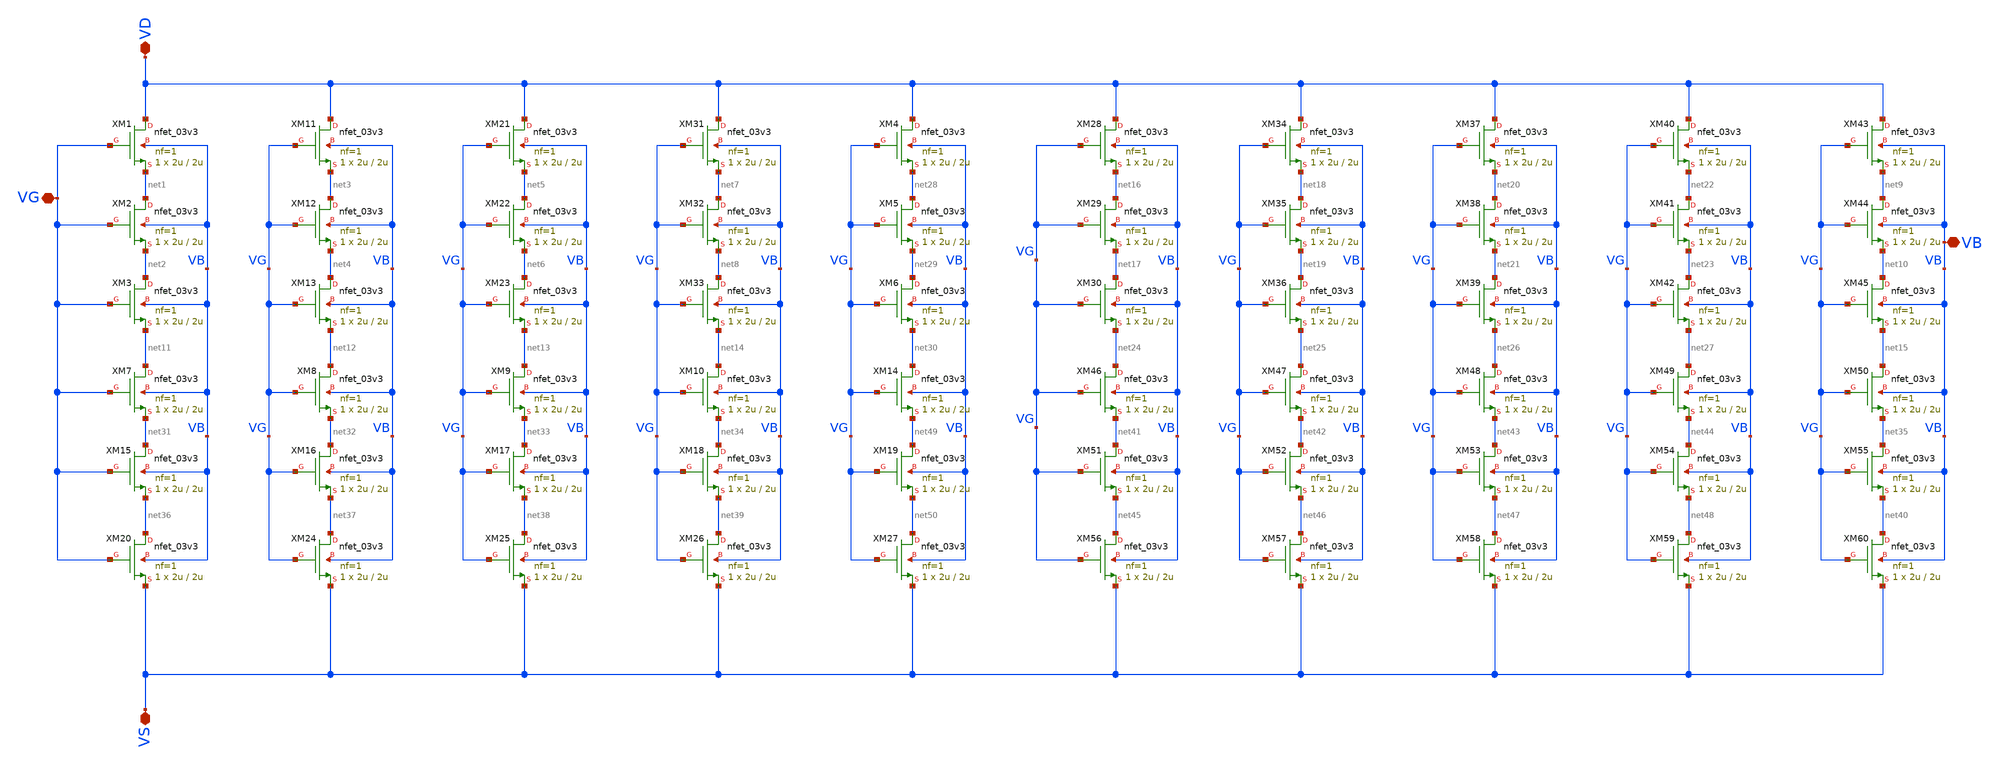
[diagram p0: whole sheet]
** sch_path: Voltage_Reference/symbols/NMOS_association_10u_6u_V2.sch
**.subckt NMOS_association_10u_6u_V2 VD VB VG VS
*.iopin VD
*.iopin VB
*.iopin VG
*.iopin VS
XM1 VD VG net1 VB nfet_03v3 L=2u W=2u nf=1 ad='int((nf+1)/2) * W/nf * 0.18u' as='int((nf+2)/2) * W/nf * 0.18u'
+ pd='2*int((nf+1)/2) * (W/nf + 0.18u)' ps='2*int((nf+2)/2) * (W/nf + 0.18u)' nrd='0.18u / W' nrs='0.18u / W'
+ sa=0 sb=0 sd=0 m=1
XM2 net1 VG net2 VB nfet_03v3 L=2u W=2u nf=1 ad='int((nf+1)/2) * W/nf * 0.18u' as='int((nf+2)/2) * W/nf * 0.18u'
+ pd='2*int((nf+1)/2) * (W/nf + 0.18u)' ps='2*int((nf+2)/2) * (W/nf + 0.18u)' nrd='0.18u / W' nrs='0.18u / W'
+ sa=0 sb=0 sd=0 m=1
XM3 net2 VG net11 VB nfet_03v3 L=2u W=2u nf=1 ad='int((nf+1)/2) * W/nf * 0.18u' as='int((nf+2)/2) * W/nf * 0.18u'
+ pd='2*int((nf+1)/2) * (W/nf + 0.18u)' ps='2*int((nf+2)/2) * (W/nf + 0.18u)' nrd='0.18u / W' nrs='0.18u / W'
+ sa=0 sb=0 sd=0 m=1
XM11 VD VG net3 VB nfet_03v3 L=2u W=2u nf=1 ad='int((nf+1)/2) * W/nf * 0.18u' as='int((nf+2)/2) * W/nf * 0.18u'
+ pd='2*int((nf+1)/2) * (W/nf + 0.18u)' ps='2*int((nf+2)/2) * (W/nf + 0.18u)' nrd='0.18u / W' nrs='0.18u / W'
+ sa=0 sb=0 sd=0 m=1
XM12 net3 VG net4 VB nfet_03v3 L=2u W=2u nf=1 ad='int((nf+1)/2) * W/nf * 0.18u' as='int((nf+2)/2) * W/nf * 0.18u'
+ pd='2*int((nf+1)/2) * (W/nf + 0.18u)' ps='2*int((nf+2)/2) * (W/nf + 0.18u)' nrd='0.18u / W' nrs='0.18u / W'
+ sa=0 sb=0 sd=0 m=1
XM13 net4 VG net12 VB nfet_03v3 L=2u W=2u nf=1 ad='int((nf+1)/2) * W/nf * 0.18u' as='int((nf+2)/2) * W/nf * 0.18u'
+ pd='2*int((nf+1)/2) * (W/nf + 0.18u)' ps='2*int((nf+2)/2) * (W/nf + 0.18u)' nrd='0.18u / W' nrs='0.18u / W'
+ sa=0 sb=0 sd=0 m=1
XM21 VD VG net5 VB nfet_03v3 L=2u W=2u nf=1 ad='int((nf+1)/2) * W/nf * 0.18u' as='int((nf+2)/2) * W/nf * 0.18u'
+ pd='2*int((nf+1)/2) * (W/nf + 0.18u)' ps='2*int((nf+2)/2) * (W/nf + 0.18u)' nrd='0.18u / W' nrs='0.18u / W'
+ sa=0 sb=0 sd=0 m=1
XM22 net5 VG net6 VB nfet_03v3 L=2u W=2u nf=1 ad='int((nf+1)/2) * W/nf * 0.18u' as='int((nf+2)/2) * W/nf * 0.18u'
+ pd='2*int((nf+1)/2) * (W/nf + 0.18u)' ps='2*int((nf+2)/2) * (W/nf + 0.18u)' nrd='0.18u / W' nrs='0.18u / W'
+ sa=0 sb=0 sd=0 m=1
XM23 net6 VG net13 VB nfet_03v3 L=2u W=2u nf=1 ad='int((nf+1)/2) * W/nf * 0.18u' as='int((nf+2)/2) * W/nf * 0.18u'
+ pd='2*int((nf+1)/2) * (W/nf + 0.18u)' ps='2*int((nf+2)/2) * (W/nf + 0.18u)' nrd='0.18u / W' nrs='0.18u / W'
+ sa=0 sb=0 sd=0 m=1
XM31 VD VG net7 VB nfet_03v3 L=2u W=2u nf=1 ad='int((nf+1)/2) * W/nf * 0.18u' as='int((nf+2)/2) * W/nf * 0.18u'
+ pd='2*int((nf+1)/2) * (W/nf + 0.18u)' ps='2*int((nf+2)/2) * (W/nf + 0.18u)' nrd='0.18u / W' nrs='0.18u / W'
+ sa=0 sb=0 sd=0 m=1
XM32 net7 VG net8 VB nfet_03v3 L=2u W=2u nf=1 ad='int((nf+1)/2) * W/nf * 0.18u' as='int((nf+2)/2) * W/nf * 0.18u'
+ pd='2*int((nf+1)/2) * (W/nf + 0.18u)' ps='2*int((nf+2)/2) * (W/nf + 0.18u)' nrd='0.18u / W' nrs='0.18u / W'
+ sa=0 sb=0 sd=0 m=1
XM33 net8 VG net14 VB nfet_03v3 L=2u W=2u nf=1 ad='int((nf+1)/2) * W/nf * 0.18u' as='int((nf+2)/2) * W/nf * 0.18u'
+ pd='2*int((nf+1)/2) * (W/nf + 0.18u)' ps='2*int((nf+2)/2) * (W/nf + 0.18u)' nrd='0.18u / W' nrs='0.18u / W'
+ sa=0 sb=0 sd=0 m=1
XM4 VD VG net28 VB nfet_03v3 L=2u W=2u nf=1 ad='int((nf+1)/2) * W/nf * 0.18u' as='int((nf+2)/2) * W/nf * 0.18u'
+ pd='2*int((nf+1)/2) * (W/nf + 0.18u)' ps='2*int((nf+2)/2) * (W/nf + 0.18u)' nrd='0.18u / W' nrs='0.18u / W'
+ sa=0 sb=0 sd=0 m=1
XM5 net28 VG net29 VB nfet_03v3 L=2u W=2u nf=1 ad='int((nf+1)/2) * W/nf * 0.18u' as='int((nf+2)/2) * W/nf * 0.18u'
+ pd='2*int((nf+1)/2) * (W/nf + 0.18u)' ps='2*int((nf+2)/2) * (W/nf + 0.18u)' nrd='0.18u / W' nrs='0.18u / W'
+ sa=0 sb=0 sd=0 m=1
XM6 net29 VG net30 VB nfet_03v3 L=2u W=2u nf=1 ad='int((nf+1)/2) * W/nf * 0.18u' as='int((nf+2)/2) * W/nf * 0.18u'
+ pd='2*int((nf+1)/2) * (W/nf + 0.18u)' ps='2*int((nf+2)/2) * (W/nf + 0.18u)' nrd='0.18u / W' nrs='0.18u / W'
+ sa=0 sb=0 sd=0 m=1
XM7 net11 VG net31 VB nfet_03v3 L=2u W=2u nf=1 ad='int((nf+1)/2) * W/nf * 0.18u' as='int((nf+2)/2) * W/nf * 0.18u'
+ pd='2*int((nf+1)/2) * (W/nf + 0.18u)' ps='2*int((nf+2)/2) * (W/nf + 0.18u)' nrd='0.18u / W' nrs='0.18u / W'
+ sa=0 sb=0 sd=0 m=1
XM8 net12 VG net32 VB nfet_03v3 L=2u W=2u nf=1 ad='int((nf+1)/2) * W/nf * 0.18u' as='int((nf+2)/2) * W/nf * 0.18u'
+ pd='2*int((nf+1)/2) * (W/nf + 0.18u)' ps='2*int((nf+2)/2) * (W/nf + 0.18u)' nrd='0.18u / W' nrs='0.18u / W'
+ sa=0 sb=0 sd=0 m=1
XM9 net13 VG net33 VB nfet_03v3 L=2u W=2u nf=1 ad='int((nf+1)/2) * W/nf * 0.18u' as='int((nf+2)/2) * W/nf * 0.18u'
+ pd='2*int((nf+1)/2) * (W/nf + 0.18u)' ps='2*int((nf+2)/2) * (W/nf + 0.18u)' nrd='0.18u / W' nrs='0.18u / W'
+ sa=0 sb=0 sd=0 m=1
XM10 net14 VG net34 VB nfet_03v3 L=2u W=2u nf=1 ad='int((nf+1)/2) * W/nf * 0.18u' as='int((nf+2)/2) * W/nf * 0.18u'
+ pd='2*int((nf+1)/2) * (W/nf + 0.18u)' ps='2*int((nf+2)/2) * (W/nf + 0.18u)' nrd='0.18u / W' nrs='0.18u / W'
+ sa=0 sb=0 sd=0 m=1
XM14 net30 VG net49 VB nfet_03v3 L=2u W=2u nf=1 ad='int((nf+1)/2) * W/nf * 0.18u' as='int((nf+2)/2) * W/nf * 0.18u'
+ pd='2*int((nf+1)/2) * (W/nf + 0.18u)' ps='2*int((nf+2)/2) * (W/nf + 0.18u)' nrd='0.18u / W' nrs='0.18u / W'
+ sa=0 sb=0 sd=0 m=1
XM28 VD VG net16 VB nfet_03v3 L=2u W=2u nf=1 ad='int((nf+1)/2) * W/nf * 0.18u' as='int((nf+2)/2) * W/nf * 0.18u'
+ pd='2*int((nf+1)/2) * (W/nf + 0.18u)' ps='2*int((nf+2)/2) * (W/nf + 0.18u)' nrd='0.18u / W' nrs='0.18u / W'
+ sa=0 sb=0 sd=0 m=1
XM29 net16 VG net17 VB nfet_03v3 L=2u W=2u nf=1 ad='int((nf+1)/2) * W/nf * 0.18u' as='int((nf+2)/2) * W/nf * 0.18u'
+ pd='2*int((nf+1)/2) * (W/nf + 0.18u)' ps='2*int((nf+2)/2) * (W/nf + 0.18u)' nrd='0.18u / W' nrs='0.18u / W'
+ sa=0 sb=0 sd=0 m=1
XM30 net17 VG net24 VB nfet_03v3 L=2u W=2u nf=1 ad='int((nf+1)/2) * W/nf * 0.18u' as='int((nf+2)/2) * W/nf * 0.18u'
+ pd='2*int((nf+1)/2) * (W/nf + 0.18u)' ps='2*int((nf+2)/2) * (W/nf + 0.18u)' nrd='0.18u / W' nrs='0.18u / W'
+ sa=0 sb=0 sd=0 m=1
XM34 VD VG net18 VB nfet_03v3 L=2u W=2u nf=1 ad='int((nf+1)/2) * W/nf * 0.18u' as='int((nf+2)/2) * W/nf * 0.18u'
+ pd='2*int((nf+1)/2) * (W/nf + 0.18u)' ps='2*int((nf+2)/2) * (W/nf + 0.18u)' nrd='0.18u / W' nrs='0.18u / W'
+ sa=0 sb=0 sd=0 m=1
XM35 net18 VG net19 VB nfet_03v3 L=2u W=2u nf=1 ad='int((nf+1)/2) * W/nf * 0.18u' as='int((nf+2)/2) * W/nf * 0.18u'
+ pd='2*int((nf+1)/2) * (W/nf + 0.18u)' ps='2*int((nf+2)/2) * (W/nf + 0.18u)' nrd='0.18u / W' nrs='0.18u / W'
+ sa=0 sb=0 sd=0 m=1
XM36 net19 VG net25 VB nfet_03v3 L=2u W=2u nf=1 ad='int((nf+1)/2) * W/nf * 0.18u' as='int((nf+2)/2) * W/nf * 0.18u'
+ pd='2*int((nf+1)/2) * (W/nf + 0.18u)' ps='2*int((nf+2)/2) * (W/nf + 0.18u)' nrd='0.18u / W' nrs='0.18u / W'
+ sa=0 sb=0 sd=0 m=1
XM37 VD VG net20 VB nfet_03v3 L=2u W=2u nf=1 ad='int((nf+1)/2) * W/nf * 0.18u' as='int((nf+2)/2) * W/nf * 0.18u'
+ pd='2*int((nf+1)/2) * (W/nf + 0.18u)' ps='2*int((nf+2)/2) * (W/nf + 0.18u)' nrd='0.18u / W' nrs='0.18u / W'
+ sa=0 sb=0 sd=0 m=1
XM38 net20 VG net21 VB nfet_03v3 L=2u W=2u nf=1 ad='int((nf+1)/2) * W/nf * 0.18u' as='int((nf+2)/2) * W/nf * 0.18u'
+ pd='2*int((nf+1)/2) * (W/nf + 0.18u)' ps='2*int((nf+2)/2) * (W/nf + 0.18u)' nrd='0.18u / W' nrs='0.18u / W'
+ sa=0 sb=0 sd=0 m=1
XM39 net21 VG net26 VB nfet_03v3 L=2u W=2u nf=1 ad='int((nf+1)/2) * W/nf * 0.18u' as='int((nf+2)/2) * W/nf * 0.18u'
+ pd='2*int((nf+1)/2) * (W/nf + 0.18u)' ps='2*int((nf+2)/2) * (W/nf + 0.18u)' nrd='0.18u / W' nrs='0.18u / W'
+ sa=0 sb=0 sd=0 m=1
XM40 VD VG net22 VB nfet_03v3 L=2u W=2u nf=1 ad='int((nf+1)/2) * W/nf * 0.18u' as='int((nf+2)/2) * W/nf * 0.18u'
+ pd='2*int((nf+1)/2) * (W/nf + 0.18u)' ps='2*int((nf+2)/2) * (W/nf + 0.18u)' nrd='0.18u / W' nrs='0.18u / W'
+ sa=0 sb=0 sd=0 m=1
XM41 net22 VG net23 VB nfet_03v3 L=2u W=2u nf=1 ad='int((nf+1)/2) * W/nf * 0.18u' as='int((nf+2)/2) * W/nf * 0.18u'
+ pd='2*int((nf+1)/2) * (W/nf + 0.18u)' ps='2*int((nf+2)/2) * (W/nf + 0.18u)' nrd='0.18u / W' nrs='0.18u / W'
+ sa=0 sb=0 sd=0 m=1
XM42 net23 VG net27 VB nfet_03v3 L=2u W=2u nf=1 ad='int((nf+1)/2) * W/nf * 0.18u' as='int((nf+2)/2) * W/nf * 0.18u'
+ pd='2*int((nf+1)/2) * (W/nf + 0.18u)' ps='2*int((nf+2)/2) * (W/nf + 0.18u)' nrd='0.18u / W' nrs='0.18u / W'
+ sa=0 sb=0 sd=0 m=1
XM43 VD VG net9 VB nfet_03v3 L=2u W=2u nf=1 ad='int((nf+1)/2) * W/nf * 0.18u' as='int((nf+2)/2) * W/nf * 0.18u'
+ pd='2*int((nf+1)/2) * (W/nf + 0.18u)' ps='2*int((nf+2)/2) * (W/nf + 0.18u)' nrd='0.18u / W' nrs='0.18u / W'
+ sa=0 sb=0 sd=0 m=1
XM44 net9 VG net10 VB nfet_03v3 L=2u W=2u nf=1 ad='int((nf+1)/2) * W/nf * 0.18u' as='int((nf+2)/2) * W/nf * 0.18u'
+ pd='2*int((nf+1)/2) * (W/nf + 0.18u)' ps='2*int((nf+2)/2) * (W/nf + 0.18u)' nrd='0.18u / W' nrs='0.18u / W'
+ sa=0 sb=0 sd=0 m=1
XM45 net10 VG net15 VB nfet_03v3 L=2u W=2u nf=1 ad='int((nf+1)/2) * W/nf * 0.18u' as='int((nf+2)/2) * W/nf * 0.18u'
+ pd='2*int((nf+1)/2) * (W/nf + 0.18u)' ps='2*int((nf+2)/2) * (W/nf + 0.18u)' nrd='0.18u / W' nrs='0.18u / W'
+ sa=0 sb=0 sd=0 m=1
XM46 net24 VG net41 VB nfet_03v3 L=2u W=2u nf=1 ad='int((nf+1)/2) * W/nf * 0.18u' as='int((nf+2)/2) * W/nf * 0.18u'
+ pd='2*int((nf+1)/2) * (W/nf + 0.18u)' ps='2*int((nf+2)/2) * (W/nf + 0.18u)' nrd='0.18u / W' nrs='0.18u / W'
+ sa=0 sb=0 sd=0 m=1
XM47 net25 VG net42 VB nfet_03v3 L=2u W=2u nf=1 ad='int((nf+1)/2) * W/nf * 0.18u' as='int((nf+2)/2) * W/nf * 0.18u'
+ pd='2*int((nf+1)/2) * (W/nf + 0.18u)' ps='2*int((nf+2)/2) * (W/nf + 0.18u)' nrd='0.18u / W' nrs='0.18u / W'
+ sa=0 sb=0 sd=0 m=1
XM48 net26 VG net43 VB nfet_03v3 L=2u W=2u nf=1 ad='int((nf+1)/2) * W/nf * 0.18u' as='int((nf+2)/2) * W/nf * 0.18u'
+ pd='2*int((nf+1)/2) * (W/nf + 0.18u)' ps='2*int((nf+2)/2) * (W/nf + 0.18u)' nrd='0.18u / W' nrs='0.18u / W'
+ sa=0 sb=0 sd=0 m=1
XM49 net27 VG net44 VB nfet_03v3 L=2u W=2u nf=1 ad='int((nf+1)/2) * W/nf * 0.18u' as='int((nf+2)/2) * W/nf * 0.18u'
+ pd='2*int((nf+1)/2) * (W/nf + 0.18u)' ps='2*int((nf+2)/2) * (W/nf + 0.18u)' nrd='0.18u / W' nrs='0.18u / W'
+ sa=0 sb=0 sd=0 m=1
XM50 net15 VG net35 VB nfet_03v3 L=2u W=2u nf=1 ad='int((nf+1)/2) * W/nf * 0.18u' as='int((nf+2)/2) * W/nf * 0.18u'
+ pd='2*int((nf+1)/2) * (W/nf + 0.18u)' ps='2*int((nf+2)/2) * (W/nf + 0.18u)' nrd='0.18u / W' nrs='0.18u / W'
+ sa=0 sb=0 sd=0 m=1
XM15 net31 VG net36 VB nfet_03v3 L=2u W=2u nf=1 ad='int((nf+1)/2) * W/nf * 0.18u' as='int((nf+2)/2) * W/nf * 0.18u'
+ pd='2*int((nf+1)/2) * (W/nf + 0.18u)' ps='2*int((nf+2)/2) * (W/nf + 0.18u)' nrd='0.18u / W' nrs='0.18u / W'
+ sa=0 sb=0 sd=0 m=1
XM16 net32 VG net37 VB nfet_03v3 L=2u W=2u nf=1 ad='int((nf+1)/2) * W/nf * 0.18u' as='int((nf+2)/2) * W/nf * 0.18u'
+ pd='2*int((nf+1)/2) * (W/nf + 0.18u)' ps='2*int((nf+2)/2) * (W/nf + 0.18u)' nrd='0.18u / W' nrs='0.18u / W'
+ sa=0 sb=0 sd=0 m=1
XM17 net33 VG net38 VB nfet_03v3 L=2u W=2u nf=1 ad='int((nf+1)/2) * W/nf * 0.18u' as='int((nf+2)/2) * W/nf * 0.18u'
+ pd='2*int((nf+1)/2) * (W/nf + 0.18u)' ps='2*int((nf+2)/2) * (W/nf + 0.18u)' nrd='0.18u / W' nrs='0.18u / W'
+ sa=0 sb=0 sd=0 m=1
XM18 net34 VG net39 VB nfet_03v3 L=2u W=2u nf=1 ad='int((nf+1)/2) * W/nf * 0.18u' as='int((nf+2)/2) * W/nf * 0.18u'
+ pd='2*int((nf+1)/2) * (W/nf + 0.18u)' ps='2*int((nf+2)/2) * (W/nf + 0.18u)' nrd='0.18u / W' nrs='0.18u / W'
+ sa=0 sb=0 sd=0 m=1
XM19 net49 VG net50 VB nfet_03v3 L=2u W=2u nf=1 ad='int((nf+1)/2) * W/nf * 0.18u' as='int((nf+2)/2) * W/nf * 0.18u'
+ pd='2*int((nf+1)/2) * (W/nf + 0.18u)' ps='2*int((nf+2)/2) * (W/nf + 0.18u)' nrd='0.18u / W' nrs='0.18u / W'
+ sa=0 sb=0 sd=0 m=1
XM20 net36 VG VS VB nfet_03v3 L=2u W=2u nf=1 ad='int((nf+1)/2) * W/nf * 0.18u' as='int((nf+2)/2) * W/nf * 0.18u'
+ pd='2*int((nf+1)/2) * (W/nf + 0.18u)' ps='2*int((nf+2)/2) * (W/nf + 0.18u)' nrd='0.18u / W' nrs='0.18u / W'
+ sa=0 sb=0 sd=0 m=1
XM24 net37 VG VS VB nfet_03v3 L=2u W=2u nf=1 ad='int((nf+1)/2) * W/nf * 0.18u' as='int((nf+2)/2) * W/nf * 0.18u'
+ pd='2*int((nf+1)/2) * (W/nf + 0.18u)' ps='2*int((nf+2)/2) * (W/nf + 0.18u)' nrd='0.18u / W' nrs='0.18u / W'
+ sa=0 sb=0 sd=0 m=1
XM25 net38 VG VS VB nfet_03v3 L=2u W=2u nf=1 ad='int((nf+1)/2) * W/nf * 0.18u' as='int((nf+2)/2) * W/nf * 0.18u'
+ pd='2*int((nf+1)/2) * (W/nf + 0.18u)' ps='2*int((nf+2)/2) * (W/nf + 0.18u)' nrd='0.18u / W' nrs='0.18u / W'
+ sa=0 sb=0 sd=0 m=1
XM26 net39 VG VS VB nfet_03v3 L=2u W=2u nf=1 ad='int((nf+1)/2) * W/nf * 0.18u' as='int((nf+2)/2) * W/nf * 0.18u'
+ pd='2*int((nf+1)/2) * (W/nf + 0.18u)' ps='2*int((nf+2)/2) * (W/nf + 0.18u)' nrd='0.18u / W' nrs='0.18u / W'
+ sa=0 sb=0 sd=0 m=1
XM27 net50 VG VS VB nfet_03v3 L=2u W=2u nf=1 ad='int((nf+1)/2) * W/nf * 0.18u' as='int((nf+2)/2) * W/nf * 0.18u'
+ pd='2*int((nf+1)/2) * (W/nf + 0.18u)' ps='2*int((nf+2)/2) * (W/nf + 0.18u)' nrd='0.18u / W' nrs='0.18u / W'
+ sa=0 sb=0 sd=0 m=1
XM51 net41 VG net45 VB nfet_03v3 L=2u W=2u nf=1 ad='int((nf+1)/2) * W/nf * 0.18u' as='int((nf+2)/2) * W/nf * 0.18u'
+ pd='2*int((nf+1)/2) * (W/nf + 0.18u)' ps='2*int((nf+2)/2) * (W/nf + 0.18u)' nrd='0.18u / W' nrs='0.18u / W'
+ sa=0 sb=0 sd=0 m=1
XM52 net42 VG net46 VB nfet_03v3 L=2u W=2u nf=1 ad='int((nf+1)/2) * W/nf * 0.18u' as='int((nf+2)/2) * W/nf * 0.18u'
+ pd='2*int((nf+1)/2) * (W/nf + 0.18u)' ps='2*int((nf+2)/2) * (W/nf + 0.18u)' nrd='0.18u / W' nrs='0.18u / W'
+ sa=0 sb=0 sd=0 m=1
XM53 net43 VG net47 VB nfet_03v3 L=2u W=2u nf=1 ad='int((nf+1)/2) * W/nf * 0.18u' as='int((nf+2)/2) * W/nf * 0.18u'
+ pd='2*int((nf+1)/2) * (W/nf + 0.18u)' ps='2*int((nf+2)/2) * (W/nf + 0.18u)' nrd='0.18u / W' nrs='0.18u / W'
+ sa=0 sb=0 sd=0 m=1
XM54 net44 VG net48 VB nfet_03v3 L=2u W=2u nf=1 ad='int((nf+1)/2) * W/nf * 0.18u' as='int((nf+2)/2) * W/nf * 0.18u'
+ pd='2*int((nf+1)/2) * (W/nf + 0.18u)' ps='2*int((nf+2)/2) * (W/nf + 0.18u)' nrd='0.18u / W' nrs='0.18u / W'
+ sa=0 sb=0 sd=0 m=1
XM55 net35 VG net40 VB nfet_03v3 L=2u W=2u nf=1 ad='int((nf+1)/2) * W/nf * 0.18u' as='int((nf+2)/2) * W/nf * 0.18u'
+ pd='2*int((nf+1)/2) * (W/nf + 0.18u)' ps='2*int((nf+2)/2) * (W/nf + 0.18u)' nrd='0.18u / W' nrs='0.18u / W'
+ sa=0 sb=0 sd=0 m=1
XM56 net45 VG VS VB nfet_03v3 L=2u W=2u nf=1 ad='int((nf+1)/2) * W/nf * 0.18u' as='int((nf+2)/2) * W/nf * 0.18u'
+ pd='2*int((nf+1)/2) * (W/nf + 0.18u)' ps='2*int((nf+2)/2) * (W/nf + 0.18u)' nrd='0.18u / W' nrs='0.18u / W'
+ sa=0 sb=0 sd=0 m=1
XM57 net46 VG VS VB nfet_03v3 L=2u W=2u nf=1 ad='int((nf+1)/2) * W/nf * 0.18u' as='int((nf+2)/2) * W/nf * 0.18u'
+ pd='2*int((nf+1)/2) * (W/nf + 0.18u)' ps='2*int((nf+2)/2) * (W/nf + 0.18u)' nrd='0.18u / W' nrs='0.18u / W'
+ sa=0 sb=0 sd=0 m=1
XM58 net47 VG VS VB nfet_03v3 L=2u W=2u nf=1 ad='int((nf+1)/2) * W/nf * 0.18u' as='int((nf+2)/2) * W/nf * 0.18u'
+ pd='2*int((nf+1)/2) * (W/nf + 0.18u)' ps='2*int((nf+2)/2) * (W/nf + 0.18u)' nrd='0.18u / W' nrs='0.18u / W'
+ sa=0 sb=0 sd=0 m=1
XM59 net48 VG VS VB nfet_03v3 L=2u W=2u nf=1 ad='int((nf+1)/2) * W/nf * 0.18u' as='int((nf+2)/2) * W/nf * 0.18u'
+ pd='2*int((nf+1)/2) * (W/nf + 0.18u)' ps='2*int((nf+2)/2) * (W/nf + 0.18u)' nrd='0.18u / W' nrs='0.18u / W'
+ sa=0 sb=0 sd=0 m=1
XM60 net40 VG VS VB nfet_03v3 L=2u W=2u nf=1 ad='int((nf+1)/2) * W/nf * 0.18u' as='int((nf+2)/2) * W/nf * 0.18u'
+ pd='2*int((nf+1)/2) * (W/nf + 0.18u)' ps='2*int((nf+2)/2) * (W/nf + 0.18u)' nrd='0.18u / W' nrs='0.18u / W'
+ sa=0 sb=0 sd=0 m=1
**.ends
.end
